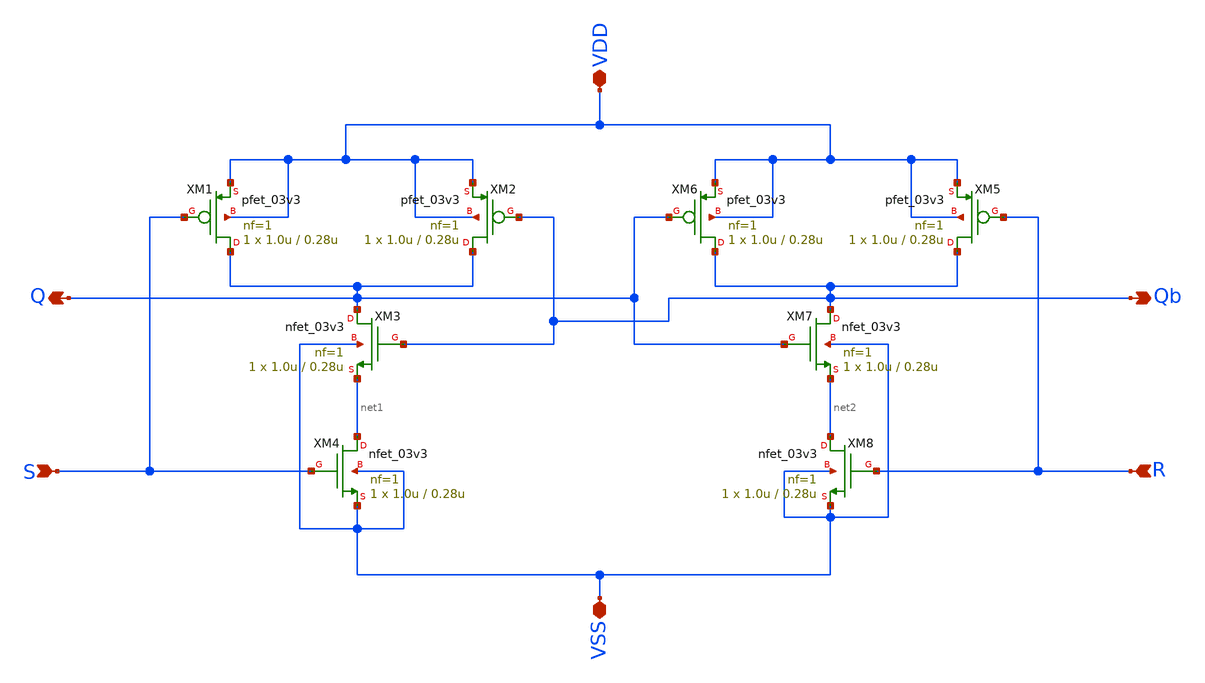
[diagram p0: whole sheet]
** sch_path: designs/libs/core_analog/nand_SR_latch/nand_SR_latch.sch
**.subckt nand_SR_latch VSS VDD S R Q Qb
*.iopin VSS
*.iopin VDD
*.ipin S
*.ipin R
*.opin Q
*.opin Qb
XM1 Q S VDD VDD pfet_03v3 L=0.28u W=1.0u nf=1 ad='int((nf+1)/2) * W/nf * 0.18u' as='int((nf+2)/2) * W/nf * 0.18u'
+ pd='2*int((nf+1)/2) * (W/nf + 0.18u)' ps='2*int((nf+2)/2) * (W/nf + 0.18u)' nrd='0.18u / W' nrs='0.18u / W'
+ sa=0 sb=0 sd=0 m=1
XM2 Q Qb VDD VDD pfet_03v3 L=0.28u W=1.0u nf=1 ad='int((nf+1)/2) * W/nf * 0.18u' as='int((nf+2)/2) * W/nf * 0.18u'
+ pd='2*int((nf+1)/2) * (W/nf + 0.18u)' ps='2*int((nf+2)/2) * (W/nf + 0.18u)' nrd='0.18u / W' nrs='0.18u / W'
+ sa=0 sb=0 sd=0 m=1
XM3 Q Qb net1 VSS nfet_03v3 L=0.28u W=1.0u nf=1 ad='int((nf+1)/2) * W/nf * 0.18u' as='int((nf+2)/2) * W/nf * 0.18u'
+ pd='2*int((nf+1)/2) * (W/nf + 0.18u)' ps='2*int((nf+2)/2) * (W/nf + 0.18u)' nrd='0.18u / W' nrs='0.18u / W'
+ sa=0 sb=0 sd=0 m=1
XM4 net1 S VSS VSS nfet_03v3 L=0.28u W=1.0u nf=1 ad='int((nf+1)/2) * W/nf * 0.18u' as='int((nf+2)/2) * W/nf * 0.18u'
+ pd='2*int((nf+1)/2) * (W/nf + 0.18u)' ps='2*int((nf+2)/2) * (W/nf + 0.18u)' nrd='0.18u / W' nrs='0.18u / W'
+ sa=0 sb=0 sd=0 m=1
XM5 Qb R VDD VDD pfet_03v3 L=0.28u W=1.0u nf=1 ad='int((nf+1)/2) * W/nf * 0.18u' as='int((nf+2)/2) * W/nf * 0.18u'
+ pd='2*int((nf+1)/2) * (W/nf + 0.18u)' ps='2*int((nf+2)/2) * (W/nf + 0.18u)' nrd='0.18u / W' nrs='0.18u / W'
+ sa=0 sb=0 sd=0 m=1
XM6 Qb Q VDD VDD pfet_03v3 L=0.28u W=1.0u nf=1 ad='int((nf+1)/2) * W/nf * 0.18u' as='int((nf+2)/2) * W/nf * 0.18u'
+ pd='2*int((nf+1)/2) * (W/nf + 0.18u)' ps='2*int((nf+2)/2) * (W/nf + 0.18u)' nrd='0.18u / W' nrs='0.18u / W'
+ sa=0 sb=0 sd=0 m=1
XM7 Qb Q net2 VSS nfet_03v3 L=0.28u W=1.0u nf=1 ad='int((nf+1)/2) * W/nf * 0.18u' as='int((nf+2)/2) * W/nf * 0.18u'
+ pd='2*int((nf+1)/2) * (W/nf + 0.18u)' ps='2*int((nf+2)/2) * (W/nf + 0.18u)' nrd='0.18u / W' nrs='0.18u / W'
+ sa=0 sb=0 sd=0 m=1
XM8 net2 R VSS VSS nfet_03v3 L=0.28u W=1.0u nf=1 ad='int((nf+1)/2) * W/nf * 0.18u' as='int((nf+2)/2) * W/nf * 0.18u'
+ pd='2*int((nf+1)/2) * (W/nf + 0.18u)' ps='2*int((nf+2)/2) * (W/nf + 0.18u)' nrd='0.18u / W' nrs='0.18u / W'
+ sa=0 sb=0 sd=0 m=1
**.ends
.end
